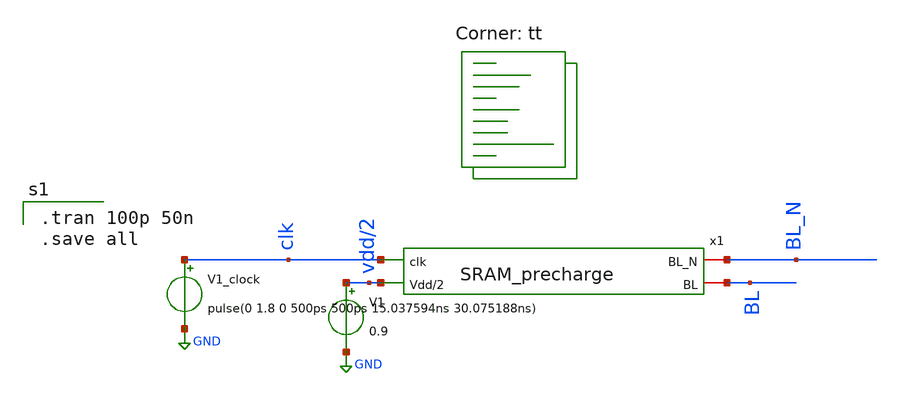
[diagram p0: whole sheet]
** sch_path: analog/schematics/precharge_tb.sch
**.subckt precharge_tb
x1 BL_N BL clk vdd/2 SRAM_precharge
V1_clock clk GND pulse(0 1.8 0 500ps 500ps 15.037594ns 30.075188ns)
V1 vdd/2 GND 0.9
**** begin user architecture code

.tran 100p 50n
.save all

.lib $::SKYWATER_MODELS/sky130.lib.spice tt
**** end user architecture code
**.ends
.GLOBAL GND
.end
